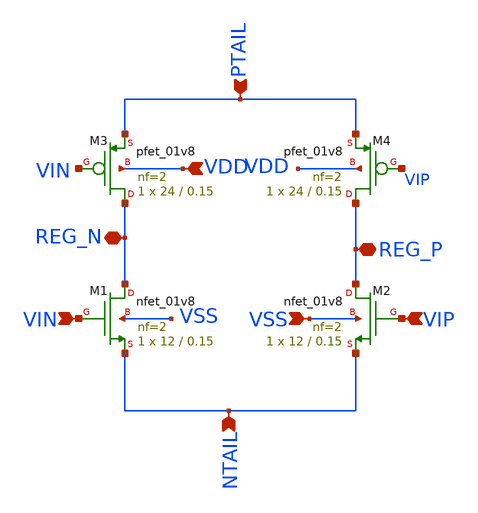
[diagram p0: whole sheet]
** sch_path: strongarm_input.sch
**.subckt strongarm_input PTAIL NTAIL REG_P REG_N VSS VDD VIP VIN
*.ipin PTAIL
*.ipin NTAIL
*.iopin REG_P
*.iopin REG_N
*.ipin VSS
*.ipin VDD
*.ipin VIP
*.ipin VIN
XM1 REG_N VIN NTAIL VSS sky130_fd_pr__nfet_01v8 L=0.15 W=12 nf=2 ad='int((2 + 1)/2) * 12 / 2 * 0.29'
+ as='int((2 + 2)/2) * 12 / 2 * 0.29' pd='2*int((2 + 1)/2) * (12 / 2 + 0.29)' ps='2*int((2 + 2)/2) * (12 / 2 + 0.29)'
+ nrd='0.29 / 12 ' nrs='0.29 / 12 ' sa=0 sb=0 sd=0 mult=1 m=1
XM2 REG_P VIP NTAIL VSS sky130_fd_pr__nfet_01v8 L=0.15 W=12 nf=2 ad='int((2 + 1)/2) * 12 / 2 * 0.29'
+ as='int((2 + 2)/2) * 12 / 2 * 0.29' pd='2*int((2 + 1)/2) * (12 / 2 + 0.29)' ps='2*int((2 + 2)/2) * (12 / 2 + 0.29)'
+ nrd='0.29 / 12 ' nrs='0.29 / 12 ' sa=0 sb=0 sd=0 mult=1 m=1
XM3 REG_N VIN PTAIL VDD sky130_fd_pr__pfet_01v8 L=0.15 W=24 nf=2 ad='int((2 + 1)/2) * 24 / 2 * 0.29'
+ as='int((2 + 2)/2) * 24 / 2 * 0.29' pd='2*int((2 + 1)/2) * (24 / 2 + 0.29)' ps='2*int((2 + 2)/2) * (24 / 2 + 0.29)'
+ nrd='0.29 / 24 ' nrs='0.29 / 24 ' sa=0 sb=0 sd=0 mult=1 m=1
XM4 REG_P VIP PTAIL VDD sky130_fd_pr__pfet_01v8 L=0.15 W=24 nf=2 ad='int((2 + 1)/2) * 24 / 2 * 0.29'
+ as='int((2 + 2)/2) * 24 / 2 * 0.29' pd='2*int((2 + 1)/2) * (24 / 2 + 0.29)' ps='2*int((2 + 2)/2) * (24 / 2 + 0.29)'
+ nrd='0.29 / 24 ' nrs='0.29 / 24 ' sa=0 sb=0 sd=0 mult=1 m=1
**.ends
.end
